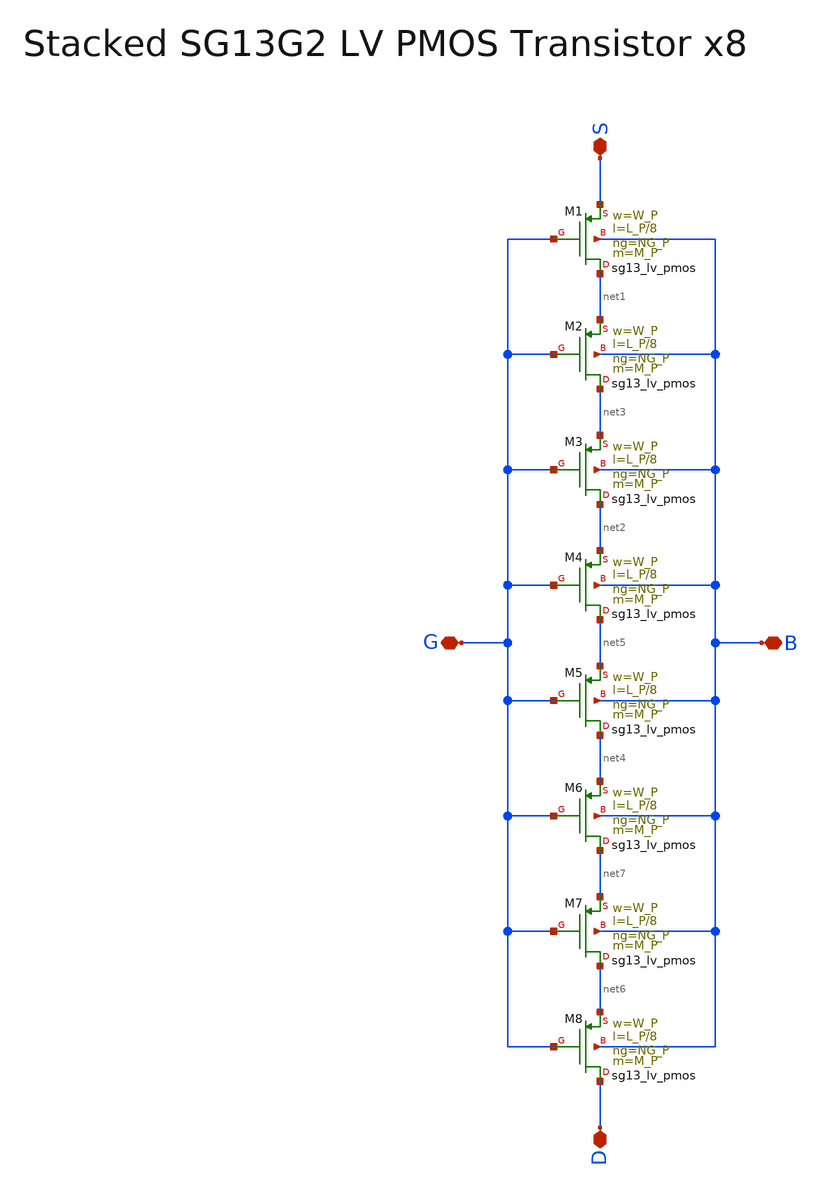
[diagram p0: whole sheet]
** sch_path: SG13G2_ATBS-ADC-main/xschem/stacked_transistors/sg13g2_lv_pmos_stacked/sg13g2_lv_pmos_stacked_x8.sch
**.subckt sg13g2_lv_pmos_stacked_x8 D S G B
*.iopin D
*.iopin S
*.iopin G
*.iopin B
XM1 net1 G S B sg13_lv_pmos w=W_P l=L_P/8 ng=NG_P m=M_P mm_ok=1
XM2 net3 G net1 B sg13_lv_pmos w=W_P l=L_P/8 ng=NG_P m=M_P mm_ok=1
XM3 net2 G net3 B sg13_lv_pmos w=W_P l=L_P/8 ng=NG_P m=M_P mm_ok=1
XM4 net5 G net2 B sg13_lv_pmos w=W_P l=L_P/8 ng=NG_P m=M_P mm_ok=1
XM5 net4 G net5 B sg13_lv_pmos w=W_P l=L_P/8 ng=NG_P m=M_P mm_ok=1
XM6 net7 G net4 B sg13_lv_pmos w=W_P l=L_P/8 ng=NG_P m=M_P mm_ok=1
XM7 net6 G net7 B sg13_lv_pmos w=W_P l=L_P/8 ng=NG_P m=M_P mm_ok=1
XM8 D G net6 B sg13_lv_pmos w=W_P l=L_P/8 ng=NG_P m=M_P mm_ok=1
**.ends
.end
